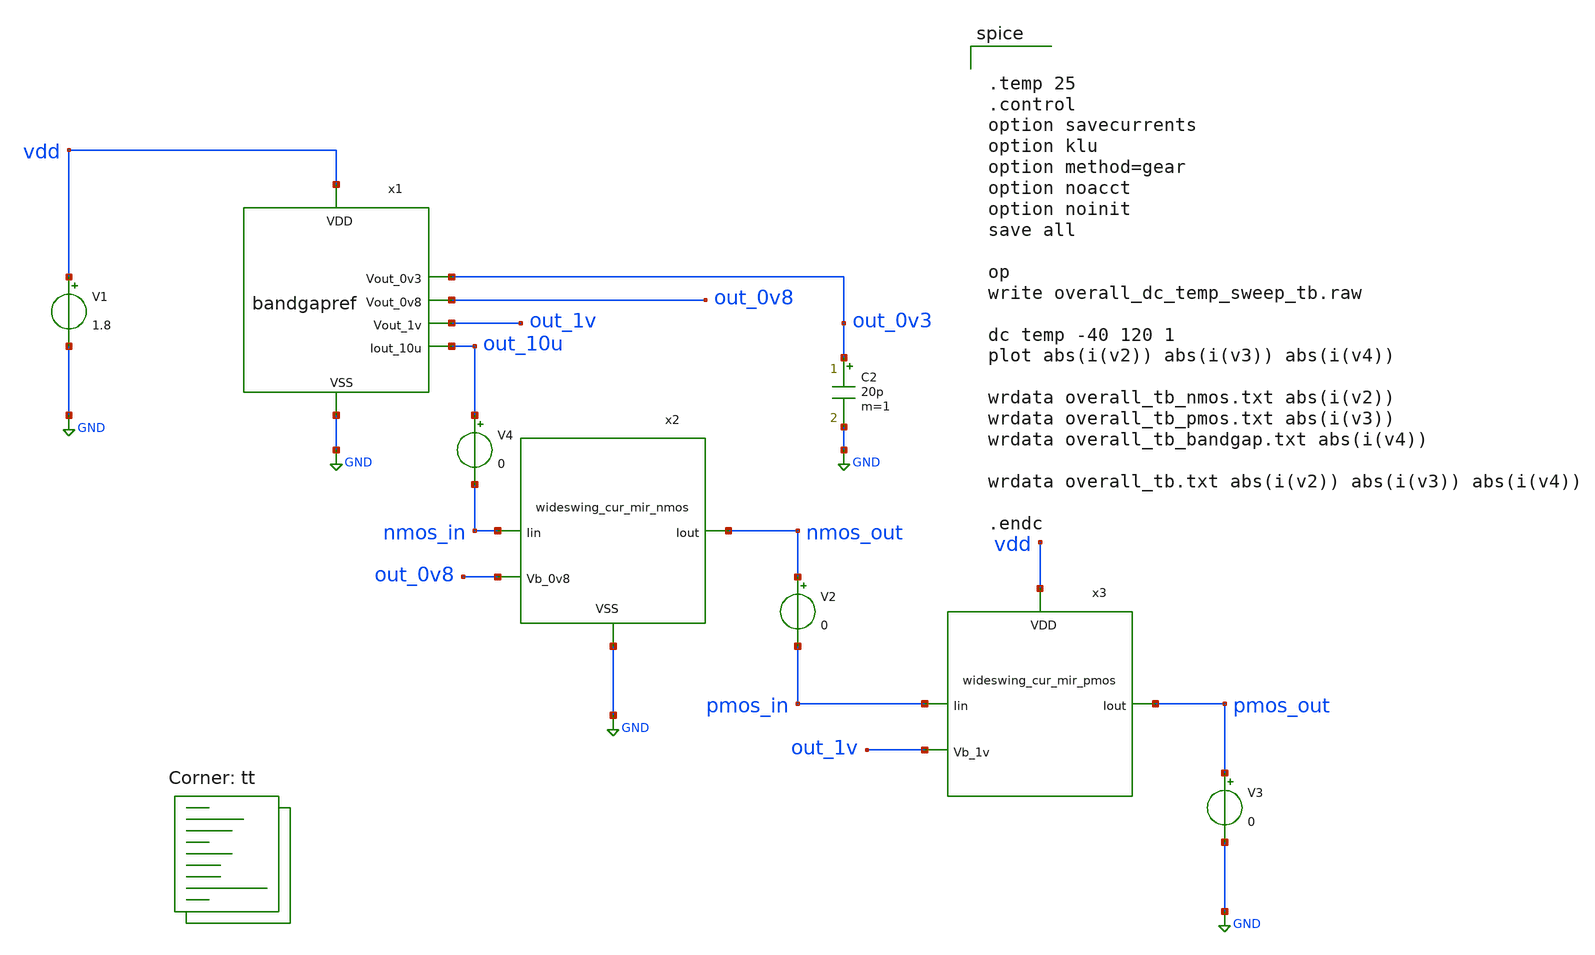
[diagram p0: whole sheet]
** sch_path: xschem/overall_dc_temp_sweep_tb.sch
**.subckt overall_dc_temp_sweep_tb
V1 vdd GND 1.8
.save i(v1)
x1 vdd out_0v3 GND out_1v out_0v8 out_10u bandgapref
C2 out_0v3 GND 20p m=1
x2 GND out_0v8 nmos_in nmos_out wideswing_cur_mir_nmos
V2 nmos_out pmos_in 0
.save i(v2)
x3 vdd out_1v pmos_in pmos_out wideswing_cur_mir_pmos
V3 pmos_out GND 0
.save i(v3)
V4 out_10u nmos_in 0
.save i(v4)
**** begin user architecture code
.lib $::SKYWATER_MODELS/sky130.lib.spice tt


.temp 25
.control
option savecurrents
option klu
option method=gear
option noacct
option noinit
save all

op
write overall_dc_temp_sweep_tb.raw

dc temp -40 120 1
plot abs(i(v2)) abs(i(v3)) abs(i(v4))

wrdata overall_tb_nmos.txt abs(i(v2))
wrdata overall_tb_pmos.txt abs(i(v3))
wrdata overall_tb_bandgap.txt abs(i(v4))

wrdata overall_tb.txt abs(i(v2)) abs(i(v3)) abs(i(v4))

.endc

**** end user architecture code
**.ends
.GLOBAL GND
.end
